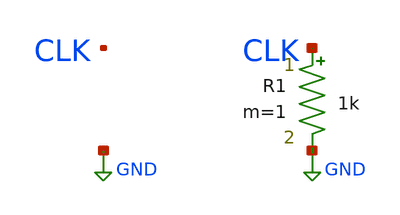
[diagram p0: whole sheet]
** sch_path: sim/jitter-calibration/testbench/tb_jitter_calibration.sch
**.subckt tb_jitter_calibration
R1 CLK GND 1k m=1
**** begin user architecture code

** GENERATED -- variant J20c: 300 cycles, nominal period
** 3.9170 ns, injected period jitter 2.000000% RMS
** (seeded RNG, seed 185020), TR = TF = 1 ns.
VCLK CLK GND pwl(  0.000000n 0 1.500000n 0 2.500000n 1.8 3.526718n 1.8  4.526718n 0 5.553435n 0
+ 6.553435n 1.8 7.554477n 1.8  8.554477n 0 9.555519n 0 10.555519n 1.8 11.516415n 1.8  12.516415n 0 13.477311n 0
+ 14.477311n 1.8 15.400017n 1.8  16.400017n 0 17.322723n 0 18.322723n 1.8 19.254881n 1.8  20.254881n 0
+ 21.187039n 0 22.187039n 1.8 23.130937n 1.8  24.130937n 0 25.074835n 0 26.074835n 1.8 27.007245n 1.8
+  28.007245n 0 28.939654n 0 29.939654n 1.8 30.911071n 1.8  31.911071n 0 32.882487n 0 33.882487n 1.8 34.881092n
+ 1.8  35.881092n 0 36.879697n 0 37.879697n 1.8 38.867873n 1.8  39.867873n 0 40.856050n 0 41.856050n 1.8
+ 42.749159n 1.8  43.749159n 0 44.642269n 0 45.642269n 1.8 46.629540n 1.8  47.629540n 0 48.616812n 0 49.616812n
+ 1.8 50.630739n 1.8  51.630739n 0 52.644665n 0 53.644665n 1.8 54.549077n 1.8  55.549077n 0 56.453489n 0
+ 57.453489n 1.8 58.452050n 1.8  59.452050n 0 60.450611n 0 61.450611n 1.8 62.322305n 1.8  63.322305n 0
+ 64.194000n 0 65.194000n 1.8 66.147324n 1.8  67.147324n 0 68.100649n 0 69.100649n 1.8 70.081258n 1.8
+  71.081258n 0 72.061868n 0 73.061868n 1.8 73.971902n 1.8  74.971902n 0 75.881936n 0 76.881936n 1.8 77.890432n
+ 1.8  78.890432n 0 79.898928n 0 80.898928n 1.8 81.849630n 1.8  82.849630n 0 83.800331n 0 84.800331n 1.8
+ 85.768505n 1.8  86.768505n 0 87.736680n 0 88.736680n 1.8 89.663668n 1.8  90.663668n 0 91.590656n 0 92.590656n
+ 1.8 93.570806n 1.8  94.570806n 0 95.550956n 0 96.550956n 1.8 97.558699n 1.8  98.558699n 0 99.566443n 0
+ 100.566443n 1.8 101.503670n 1.8  102.503670n 0 103.440896n 0 104.440896n 1.8 105.348168n 1.8  106.348168n 0
+ 107.255440n 0 108.255440n 1.8 109.127216n 1.8  110.127216n 0 110.998993n 0 111.998993n 1.8 112.991125n 1.8
+  113.991125n 0 114.983257n 0 115.983257n 1.8 116.928776n 1.8  117.928776n 0 118.874294n 0 119.874294n 1.8
+ 120.865963n 1.8  121.865963n 0 122.857631n 0 123.857631n 1.8 124.819040n 1.8  125.819040n 0 126.780448n 0
+ 127.780448n 1.8 128.706747n 1.8  129.706747n 0 130.633045n 0 131.633045n 1.8 132.625448n 1.8  133.625448n 0
+ 134.617851n 0 135.617851n 1.8 136.632783n 1.8  137.632783n 0 138.647715n 0 139.647715n 1.8 140.640677n 1.8
+  141.640677n 0 142.633638n 0 143.633638n 1.8 144.598818n 1.8  145.598818n 0 146.563997n 0 147.563997n 1.8
+ 148.479751n 1.8  149.479751n 0 150.395504n 0 151.395504n 1.8 152.395248n 1.8  153.395248n 0 154.394992n 0
+ 155.394992n 1.8 156.346499n 1.8  157.346499n 0 158.298005n 0 159.298005n 1.8 160.186095n 1.8  161.186095n 0
+ 162.074185n 0 163.074185n 1.8 164.026918n 1.8  165.026918n 0 165.979650n 0 166.979650n 1.8 167.883842n 1.8
+  168.883842n 0 169.788033n 0 170.788033n 1.8 171.799283n 1.8  172.799283n 0 173.810533n 0 174.810533n 1.8
+ 175.796602n 1.8  176.796602n 0 177.782670n 0 178.782670n 1.8 179.685998n 1.8  180.685998n 0 181.589326n 0
+ 182.589326n 1.8 183.589354n 1.8  184.589354n 0 185.589381n 0 186.589381n 1.8 187.571504n 1.8  188.571504n 0
+ 189.553627n 0 190.553627n 1.8 191.511032n 1.8  192.511032n 0 193.468436n 0 194.468436n 1.8 195.394042n 1.8
+  196.394042n 0 197.319648n 0 198.319648n 1.8 199.208880n 1.8  200.208880n 0 201.098112n 0 202.098112n 1.8
+ 203.092624n 1.8  204.092624n 0 205.087135n 0 206.087135n 1.8 207.038938n 1.8  208.038938n 0 208.990741n 0
+ 209.990741n 1.8 210.960868n 1.8  211.960868n 0 212.930995n 0 213.930995n 1.8 214.853427n 1.8  215.853427n 0
+ 216.775859n 0 217.775859n 1.8 218.742708n 1.8  219.742708n 0 220.709557n 0 221.709557n 1.8 222.685296n 1.8
+  223.685296n 0 224.661034n 0 225.661034n 1.8 226.636825n 1.8  227.636825n 0 228.612615n 0 229.612615n 1.8
+ 230.605090n 1.8  231.605090n 0 232.597564n 0 233.597564n 1.8 234.630977n 1.8  235.630977n 0 236.664390n 0
+ 237.664390n 1.8 238.560409n 1.8  239.560409n 0 240.456429n 0 241.456429n 1.8 242.409372n 1.8  243.409372n 0
+ 244.362314n 0 245.362314n 1.8 246.346034n 1.8  247.346034n 0 248.329753n 0 249.329753n 1.8 250.273425n 1.8
+  251.273425n 0 252.217097n 0 253.217097n 1.8 254.173888n 1.8  255.173888n 0 256.130679n 0 257.130679n 1.8
+ 258.076368n 1.8  259.076368n 0 260.022057n 0 261.022057n 1.8 262.054386n 1.8  263.054386n 0 264.086716n 0
+ 265.086716n 1.8 266.050911n 1.8  267.050911n 0 268.015107n 0 269.015107n 1.8 269.990510n 1.8  270.990510n 0
+ 271.965913n 0 272.965913n 1.8 273.950816n 1.8  274.950816n 0 275.935719n 0 276.935719n 1.8 277.856576n 1.8
+  278.856576n 0 279.777433n 0 280.777433n 1.8 281.770433n 1.8  282.770433n 0 283.763434n 0 284.763434n 1.8
+ 285.726767n 1.8  286.726767n 0 287.690100n 0 288.690100n 1.8 289.584317n 1.8  290.584317n 0 291.478534n 0
+ 292.478534n 1.8 293.481446n 1.8  294.481446n 0 295.484358n 0 296.484358n 1.8 297.421955n 1.8  298.421955n 0
+ 299.359553n 0 300.359553n 1.8 301.288550n 1.8  302.288550n 0 303.217548n 0 304.217548n 1.8 305.206708n 1.8
+  306.206708n 0 307.195869n 0 308.195869n 1.8 309.111346n 1.8  310.111346n 0 311.026824n 0 312.026824n 1.8
+ 313.068151n 1.8  314.068151n 0 315.109479n 0 316.109479n 1.8 316.978904n 1.8  317.978904n 0 318.848329n 0
+ 319.848329n 1.8 320.796071n 1.8  321.796071n 0 322.743813n 0 323.743813n 1.8 324.785839n 1.8  325.785839n 0
+ 326.827866n 0 327.827866n 1.8 328.711935n 1.8  329.711935n 0 330.596004n 0 331.596004n 1.8 332.503577n 1.8
+  333.503577n 0 334.411150n 0 335.411150n 1.8 336.404651n 1.8  337.404651n 0 338.398152n 0 339.398152n 1.8
+ 340.343668n 1.8  341.343668n 0 342.289183n 0 343.289183n 1.8 344.243582n 1.8  345.243582n 0 346.197980n 0
+ 347.197980n 1.8 348.187998n 1.8  349.187998n 0 350.178017n 0 351.178017n 1.8 352.160082n 1.8  353.160082n 0
+ 354.142147n 0 355.142147n 1.8 356.122866n 1.8  357.122866n 0 358.103585n 0 359.103585n 1.8 360.059817n 1.8
+  361.059817n 0 362.016049n 0 363.016049n 1.8 363.955060n 1.8  364.955060n 0 365.894070n 0 366.894070n 1.8
+ 367.788905n 1.8  368.788905n 0 369.683740n 0 370.683740n 1.8 371.639765n 1.8  372.639765n 0 373.595790n 0
+ 374.595790n 1.8 375.555147n 1.8  376.555147n 0 377.514503n 0 378.514503n 1.8 379.462582n 1.8  380.462582n 0
+ 381.410661n 0 382.410661n 1.8 383.319276n 1.8  384.319276n 0 385.227892n 0 386.227892n 1.8 387.187304n 1.8
+  388.187304n 0 389.146716n 0 390.146716n 1.8 391.206628n 1.8  392.206628n 0 393.266540n 0 394.266540n 1.8
+ 395.205526n 1.8  396.205526n 0 397.144512n 0 398.144512n 1.8 399.055598n 1.8  400.055598n 0 400.966683n 0
+ 401.966683n 1.8 402.949484n 1.8  403.949484n 0 404.932285n 0 405.932285n 1.8 406.816987n 1.8  407.816987n 0
+ 408.701689n 0 409.701689n 1.8 410.616584n 1.8  411.616584n 0 412.531480n 0 413.531480n 1.8 414.445456n 1.8
+  415.445456n 0 416.359433n 0 417.359433n 1.8 418.324902n 1.8  419.324902n 0 420.290371n 0 421.290371n 1.8
+ 422.174743n 1.8  423.174743n 0 424.059115n 0 425.059115n 1.8 426.036184n 1.8  427.036184n 0 428.013253n 0
+ 429.013253n 1.8 429.910539n 1.8  430.910539n 0 431.807825n 0 432.807825n 1.8 433.776575n 1.8  434.776575n 0
+ 435.745325n 0 436.745325n 1.8 437.720629n 1.8  438.720629n 0 439.695933n 0 440.695933n 1.8 441.682729n 1.8
+  442.682729n 0 443.669524n 0 444.669524n 1.8 445.598918n 1.8  446.598918n 0 447.528311n 0 448.528311n 1.8
+ 449.479560n 1.8  450.479560n 0 451.430810n 0 452.430810n 1.8 453.383011n 1.8  454.383011n 0 455.335213n 0
+ 456.335213n 1.8 457.333733n 1.8  458.333733n 0 459.332254n 0 460.332254n 1.8 461.322428n 1.8  462.322428n 0
+ 463.312602n 0 464.312602n 1.8 465.280601n 1.8  466.280601n 0 467.248600n 0 468.248600n 1.8 469.168893n 1.8
+  470.168893n 0 471.089186n 0 472.089186n 1.8 473.096590n 1.8  474.096590n 0 475.103993n 0 476.103993n 1.8
+ 477.077030n 1.8  478.077030n 0 479.050068n 0 480.050068n 1.8 480.999655n 1.8  481.999655n 0 482.949242n 0
+ 483.949242n 1.8 484.936479n 1.8  485.936479n 0 486.923716n 0 487.923716n 1.8 488.891229n 1.8  489.891229n 0
+ 490.858743n 0 491.858743n 1.8 492.869815n 1.8  493.869815n 0 494.880888n 0 495.880888n 1.8 496.834749n 1.8
+  497.834749n 0 498.788611n 0 499.788611n 1.8 500.811995n 1.8  501.811995n 0 502.835378n 0 503.835378n 1.8
+ 504.858923n 1.8  505.858923n 0 506.882469n 0 507.882469n 1.8 508.809741n 1.8  509.809741n 0 510.737014n 0
+ 511.737014n 1.8 512.716577n 1.8  513.716577n 0 514.696139n 0 515.696139n 1.8 516.675999n 1.8  517.675999n 0
+ 518.655858n 0 519.655858n 1.8 520.618706n 1.8  521.618706n 0 522.581554n 0 523.581554n 1.8 524.554875n 1.8
+  525.554875n 0 526.528197n 0 527.528197n 1.8 528.537620n 1.8  529.537620n 0 530.547044n 0 531.547044n 1.8
+ 532.556717n 1.8  533.556717n 0 534.566390n 0 535.566390n 1.8 536.584310n 1.8  537.584310n 0 538.602230n 0
+ 539.602230n 1.8 540.583828n 1.8  541.583828n 0 542.565426n 0 543.565426n 1.8 544.493725n 1.8  545.493725n 0
+ 546.422023n 0 547.422023n 1.8 548.397184n 1.8  549.397184n 0 550.372344n 0 551.372344n 1.8 552.307766n 1.8
+  553.307766n 0 554.243188n 0 555.243188n 1.8 556.226902n 1.8  557.226902n 0 558.210615n 0 559.210615n 1.8
+ 560.198627n 1.8  561.198627n 0 562.186639n 0 563.186639n 1.8 564.209040n 1.8  565.209040n 0 566.231442n 0
+ 567.231442n 1.8 568.169672n 1.8  569.169672n 0 570.107902n 0 571.107902n 1.8 572.076745n 1.8  573.076745n 0
+ 574.045589n 0 575.045589n 1.8 575.971496n 1.8  576.971496n 0 577.897402n 0 578.897402n 1.8 579.927165n 1.8
+  580.927165n 0 581.956927n 0 582.956927n 1.8 583.909947n 1.8  584.909947n 0 585.862966n 0 586.862966n 1.8
+ 587.819133n 1.8  588.819133n 0 589.775300n 0 590.775300n 1.8 591.740087n 1.8  592.740087n 0 593.704873n 0
+ 594.704873n 1.8 595.662320n 1.8  596.662320n 0 597.619766n 0 598.619766n 1.8 599.529310n 1.8  600.529310n 0
+ 601.438854n 0 602.438854n 1.8 603.439334n 1.8  604.439334n 0 605.439814n 0 606.439814n 1.8 607.374491n 1.8
+  608.374491n 0 609.309167n 0 610.309167n 1.8 611.222369n 1.8  612.222369n 0 613.135571n 0 614.135571n 1.8
+ 615.116797n 1.8  616.116797n 0 617.098023n 0 618.098023n 1.8 619.101911n 1.8  620.101911n 0 621.105799n 0
+ 622.105799n 1.8 623.101510n 1.8  624.101510n 0 625.097220n 0 626.097220n 1.8 627.076144n 1.8  628.076144n 0
+ 629.055068n 0 630.055068n 1.8 630.984426n 1.8  631.984426n 0 632.913784n 0 633.913784n 1.8 634.800661n 1.8
+  635.800661n 0 636.687537n 0 637.687537n 1.8 638.629021n 1.8  639.629021n 0 640.570504n 0 641.570504n 1.8
+ 642.498441n 1.8  643.498441n 0 644.426379n 0 645.426379n 1.8 646.421783n 1.8  647.421783n 0 648.417187n 0
+ 649.417187n 1.8 650.396993n 1.8  651.396993n 0 652.376798n 0 653.376798n 1.8 654.381530n 1.8  655.381530n 0
+ 656.386262n 0 657.386262n 1.8 658.293018n 1.8  659.293018n 0 660.199774n 0 661.199774n 1.8 662.181867n 1.8
+  663.181867n 0 664.163959n 0 665.163959n 1.8 666.152698n 1.8  667.152698n 0 668.141437n 0 669.141437n 1.8
+ 670.043424n 1.8  671.043424n 0 671.945410n 0 672.945410n 1.8 673.919042n 1.8  674.919042n 0 675.892674n 0
+ 676.892674n 1.8 677.882503n 1.8  678.882503n 0 679.872333n 0 680.872333n 1.8 681.859271n 1.8  682.859271n 0
+ 683.846208n 0 684.846208n 1.8 685.785469n 1.8  686.785469n 0 687.724729n 0 688.724729n 1.8 689.675530n 1.8
+  690.675530n 0 691.626332n 0 692.626332n 1.8 693.589827n 1.8  694.589827n 0 695.553322n 0 696.553322n 1.8
+ 697.484842n 1.8  698.484842n 0 699.416363n 0 700.416363n 1.8 701.364123n 1.8  702.364123n 0 703.311883n 0
+ 704.311883n 1.8 705.261815n 1.8  706.261815n 0 707.211747n 0 708.211747n 1.8 709.162950n 1.8  710.162950n 0
+ 711.114153n 0 712.114153n 1.8 713.070599n 1.8  714.070599n 0 715.027045n 0 716.027045n 1.8 717.021793n 1.8
+  718.021793n 0 719.016540n 0 720.016540n 1.8 720.933188n 1.8  721.933188n 0 722.849836n 0 723.849836n 1.8
+ 724.794470n 1.8  725.794470n 0 726.739103n 0 727.739103n 1.8 728.658581n 1.8  729.658581n 0 730.578058n 0
+ 731.578058n 1.8 732.464673n 1.8  733.464673n 0 734.351287n 0 735.351287n 1.8 736.298530n 1.8  737.298530n 0
+ 738.245773n 0 739.245773n 1.8 740.171536n 1.8  741.171536n 0 742.097299n 0 743.097299n 1.8 744.059487n 1.8
+  745.059487n 0 746.021676n 0 747.021676n 1.8 747.978433n 1.8  748.978433n 0 749.935190n 0 750.935190n 1.8
+ 751.831361n 1.8  752.831361n 0 753.727532n 0 754.727532n 1.8 755.652395n 1.8  756.652395n 0 757.577257n 0
+ 758.577257n 1.8 759.532181n 1.8  760.532181n 0 761.487105n 0 762.487105n 1.8 763.472876n 1.8  764.472876n 0
+ 765.458646n 0 766.458646n 1.8 767.421526n 1.8  768.421526n 0 769.384406n 0 770.384406n 1.8 771.331382n 1.8
+  772.331382n 0 773.278359n 0 774.278359n 1.8 775.202756n 1.8  776.202756n 0 777.127154n 0 778.127154n 1.8
+ 779.113196n 1.8  780.113196n 0 781.099237n 0 782.099237n 1.8 783.071057n 1.8  784.071057n 0 785.042876n 0
+ 786.042876n 1.8 787.017634n 1.8  788.017634n 0 788.992391n 0 789.992391n 1.8 790.979367n 1.8  791.979367n 0
+ 792.966343n 0 793.966343n 1.8 794.924664n 1.8  795.924664n 0 796.882985n 0 797.882985n 1.8 798.925909n 1.8
+  799.925909n 0 800.968833n 0 801.968833n 1.8 802.920192n 1.8  803.920192n 0 804.871552n 0 805.871552n 1.8
+ 806.867617n 1.8  807.867617n 0 808.863681n 0 809.863681n 1.8 810.841412n 1.8  811.841412n 0 812.819143n 0
+ 813.819143n 1.8 814.752398n 1.8  815.752398n 0 816.685652n 0 817.685652n 1.8 818.689165n 1.8  819.689165n 0
+ 820.692678n 0 821.692678n 1.8 822.677197n 1.8  823.677197n 0 824.661717n 0 825.661717n 1.8 826.616711n 1.8
+  827.616711n 0 828.571704n 0 829.571704n 1.8 830.452478n 1.8  831.452478n 0 832.333252n 0 833.333252n 1.8
+ 834.311668n 1.8  835.311668n 0 836.290084n 0 837.290084n 1.8 838.258341n 1.8  839.258341n 0 840.226598n 0
+ 841.226598n 1.8 842.137197n 1.8  843.137197n 0 844.047795n 0 845.047795n 1.8 846.060141n 1.8  847.060141n 0
+ 848.072487n 0 849.072487n 1.8 849.991148n 1.8  850.991148n 0 851.909810n 0 852.909810n 1.8 853.924838n 1.8
+  854.924838n 0 855.939866n 0 856.939866n 1.8 857.870589n 1.8  858.870589n 0 859.801313n 0 860.801313n 1.8
+ 861.767161n 1.8  862.767161n 0 863.733009n 0 864.733009n 1.8 865.694170n 1.8  866.694170n 0 867.655331n 0
+ 868.655331n 1.8 869.629893n 1.8  870.629893n 0 871.604455n 0 872.604455n 1.8 873.474315n 1.8  874.474315n 0
+ 875.344175n 0 876.344175n 1.8 877.253680n 1.8  878.253680n 0 879.163185n 0 880.163185n 1.8 881.164700n 1.8
+  882.164700n 0 883.166216n 0 884.166216n 1.8 885.105035n 1.8  886.105035n 0 887.043854n 0 888.043854n 1.8
+ 889.082929n 1.8  890.082929n 0 891.122005n 0 892.122005n 1.8 893.092369n 1.8  894.092369n 0 895.062733n 0
+ 896.062733n 1.8 896.987649n 1.8  897.987649n 0 898.912565n 0 899.912565n 1.8 900.917191n 1.8  901.917191n 0
+ 902.921817n 0 903.921817n 1.8 904.923546n 1.8  905.923546n 0 906.925274n 0 907.925274n 1.8 908.907789n 1.8
+  909.907789n 0 910.890304n 0 911.890304n 1.8 912.875516n 1.8  913.875516n 0 914.860727n 0 915.860727n 1.8
+ 916.904989n 1.8  917.904989n 0 918.949251n 0 919.949251n 1.8 920.886669n 1.8  921.886669n 0 922.824087n 0
+ 923.824087n 1.8 924.818395n 1.8  925.818395n 0 926.812702n 0 927.812702n 1.8 928.762797n 1.8  929.762797n 0
+ 930.712893n 0 931.712893n 1.8 932.701082n 1.8  933.701082n 0 934.689271n 0 935.689271n 1.8 936.694494n 1.8
+  937.694494n 0 938.699717n 0 939.699717n 1.8 940.635642n 1.8  941.635642n 0 942.571567n 0 943.571567n 1.8
+ 944.503490n 1.8  945.503490n 0 946.435412n 0 947.435412n 1.8 948.363839n 1.8  949.363839n 0 950.292266n 0
+ 951.292266n 1.8 952.246392n 1.8  953.246392n 0 954.200518n 0 955.200518n 1.8 956.126896n 1.8  957.126896n 0
+ 958.053274n 0 959.053274n 1.8 959.872585n 1.8  960.872585n 0 961.691896n 0 962.691896n 1.8 963.664953n 1.8
+  964.664953n 0 965.638009n 0 966.638009n 1.8 967.591215n 1.8  968.591215n 0 969.544420n 0 970.544420n 1.8
+ 971.480280n 1.8  972.480280n 0 973.416139n 0 974.416139n 1.8 975.304763n 1.8  976.304763n 0 977.193386n 0
+ 978.193386n 1.8 979.107186n 1.8  980.107186n 0 981.020987n 0 982.020987n 1.8 982.924699n 1.8  983.924699n 0
+ 984.828411n 0 985.828411n 1.8 986.807940n 1.8  987.807940n 0 988.787469n 0 989.787469n 1.8 990.760144n 1.8
+  991.760144n 0 992.732818n 0 993.732818n 1.8 994.700999n 1.8  995.700999n 0 996.669180n 0 997.669180n 1.8
+ 998.628120n 1.8  999.628120n 0 1000.587060n 0 1001.587060n 1.8 1002.529660n 1.8  1003.529660n 0 1004.472259n 0
+ 1005.472259n 1.8 1006.425794n 1.8  1007.425794n 0 1008.379329n 0 1009.379329n 1.8 1010.234314n 1.8  1011.234314n
+ 0 1012.089298n 0 1013.089298n 1.8 1014.076840n 1.8  1015.076840n 0 1016.064383n 0 1017.064383n 1.8
+ 1017.962444n 1.8  1018.962444n 0 1019.860505n 0 1020.860505n 1.8 1021.813828n 1.8  1022.813828n 0 1023.767150n 0
+ 1024.767150n 1.8 1025.700931n 1.8  1026.700931n 0 1027.634712n 0 1028.634712n 1.8 1029.553101n 1.8  1030.553101n
+ 0 1031.471489n 0 1032.471489n 1.8 1033.464841n 1.8  1034.464841n 0 1035.458194n 0 1036.458194n 1.8
+ 1037.484863n 1.8  1038.484863n 0 1039.511532n 0 1040.511532n 1.8 1041.470865n 1.8  1042.470865n 0 1043.430197n 0
+ 1044.430197n 1.8 1045.381948n 1.8  1046.381948n 0 1047.333699n 0 1048.333699n 1.8 1049.207733n 1.8  1050.207733n
+ 0 1051.081766n 0 1052.081766n 1.8 1053.071904n 1.8  1054.071904n 0 1055.062041n 0 1056.062041n 1.8
+ 1056.961843n 1.8  1057.961843n 0 1058.861646n 0 1059.861646n 1.8 1060.840990n 1.8  1061.840990n 0 1062.820334n 0
+ 1063.820334n 1.8 1064.850804n 1.8  1065.850804n 0 1066.881275n 0 1067.881275n 1.8 1068.886057n 1.8  1069.886057n
+ 0 1070.890838n 0 1071.890838n 1.8 1072.894127n 1.8  1073.894127n 0 1074.897415n 0 1075.897415n 1.8
+ 1076.786152n 1.8  1077.786152n 0 1078.674889n 0 1079.674889n 1.8 1080.669770n 1.8  1081.669770n 0 1082.664651n 0
+ 1083.664651n 1.8 1084.632823n 1.8  1085.632823n 0 1086.600996n 0 1087.600996n 1.8 1088.529023n 1.8  1089.529023n
+ 0 1090.457050n 0 1091.457050n 1.8 1092.428508n 1.8  1093.428508n 0 1094.399967n 0 1095.399967n 1.8
+ 1096.346147n 1.8  1097.346147n 0 1098.292327n 0 1099.292327n 1.8 1100.262081n 1.8  1101.262081n 0 1102.231836n 0
+ 1103.231836n 1.8 1104.152715n 1.8  1105.152715n 0 1106.073594n 0 1107.073594n 1.8 1108.032064n 1.8  1109.032064n
+ 0 1109.990534n 0 1110.990534n 1.8 1111.968346n 1.8  1112.968346n 0 1113.946158n 0 1114.946158n 1.8
+ 1115.952095n 1.8  1116.952095n 0 1117.958032n 0 1118.958032n 1.8 1119.923233n 1.8  1120.923233n 0 1121.888434n 0
+ 1122.888434n 1.8 1123.830813n 1.8  1124.830813n 0 1125.773193n 0 1126.773193n 1.8 1127.770548n 1.8  1128.770548n
+ 0 1129.767902n 0 1130.767902n 1.8 1131.689554n 1.8  1132.689554n 0 1133.611205n 0 1134.611205n 1.8
+ 1135.591027n 1.8  1136.591027n 0 1137.570849n 0 1138.570849n 1.8 1139.489201n 1.8  1140.489201n 0 1141.407553n 0
+ 1142.407553n 1.8 1143.370904n 1.8  1144.370904n 0 1145.334255n 0 1146.334255n 1.8 1147.310668n 1.8  1148.310668n
+ 0 1149.287081n 0 1150.287081n 1.8 1151.229362n 1.8  1152.229362n 0 1153.171642n 0 1154.171642n 1.8
+ 1155.141985n 1.8  1156.141985n 0 1157.112328n 0 1158.112328n 1.8 1159.058217n 1.8  1160.058217n 0 1161.004106n 0
+ 1162.004106n 1.8 1162.956936n 1.8  1163.956936n 0 1164.909766n 0 1165.909766n 1.8 1166.862340n 1.8  1167.862340n
+ 0 1168.814913n 0 1169.814913n 1.8 1170.778943n 1.8  1171.778943n 0 1172.742972n 0 1173.742972n 1.8
+ 1174.671486n 1.8  1175.671486n 0 1176.600000n 0 1177.600000n 1.8 1178.558500n 1.8  1179.558500n 0  )


** sky130 PDK model include (tt corner) -- patched per-point by sim/harness.
** No device in this testbench uses it: it is here so the harness's own
** corner substitution and this record's environment provenance are the same
** as every other campaign's. See this file's header comment.
.lib $::SKYWATER_MODELS/sky130.lib.spice tt
** No .tran/.print card here on purpose -- sim/harness/measure.py injects the
** analysis from this manifest's own measure block.

**** end user architecture code
**.ends
.GLOBAL GND
.end
